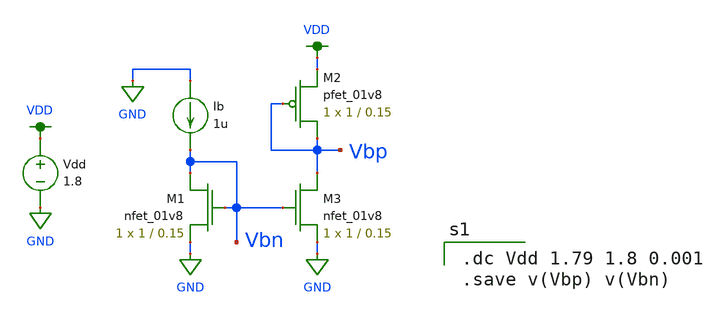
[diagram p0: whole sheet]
** sch_path: MP3/xschem/test.sch
**.subckt test
Vdd VDD GND 1.8
XM1 Vbn Vbn GND GND sky130_fd_pr__nfet_01v8 L=0.15 W=1 nf=1 ad='int((nf+1)/2) * W/nf * 0.29' as='int((nf+2)/2) * W/nf * 0.29'
+ pd='2*int((nf+1)/2) * (W/nf + 0.29)' ps='2*int((nf+2)/2) * (W/nf + 0.29)' nrd='0.29 / W' nrs='0.29 / W'
+ sa=0 sb=0 sd=0 mult=1 m=1
XM2 Vbp Vbp VDD VDD sky130_fd_pr__pfet_01v8 L=0.15 W=1 nf=1 ad='int((nf+1)/2) * W/nf * 0.29' as='int((nf+2)/2) * W/nf * 0.29'
+ pd='2*int((nf+1)/2) * (W/nf + 0.29)' ps='2*int((nf+2)/2) * (W/nf + 0.29)' nrd='0.29 / W' nrs='0.29 / W'
+ sa=0 sb=0 sd=0 mult=1 m=1
XM3 Vbp Vbn GND GND sky130_fd_pr__nfet_01v8 L=0.15 W=1 nf=1 ad='int((nf+1)/2) * W/nf * 0.29' as='int((nf+2)/2) * W/nf * 0.29'
+ pd='2*int((nf+1)/2) * (W/nf + 0.29)' ps='2*int((nf+2)/2) * (W/nf + 0.29)' nrd='0.29 / W' nrs='0.29 / W'
+ sa=0 sb=0 sd=0 mult=1 m=1
Ib GND Vbn 1u
**** begin user architecture code

.option wnflag=1
.lib ~/skywater/skywater-pdk/libraries/sky130_fd_pr_ngspice/latest/models/sky130.lib.spice tt


.dc Vdd 1.79 1.8 0.001
.save v(Vbp) v(Vbn)

**** end user architecture code
**.ends
.GLOBAL GND
.GLOBAL VDD
.end
